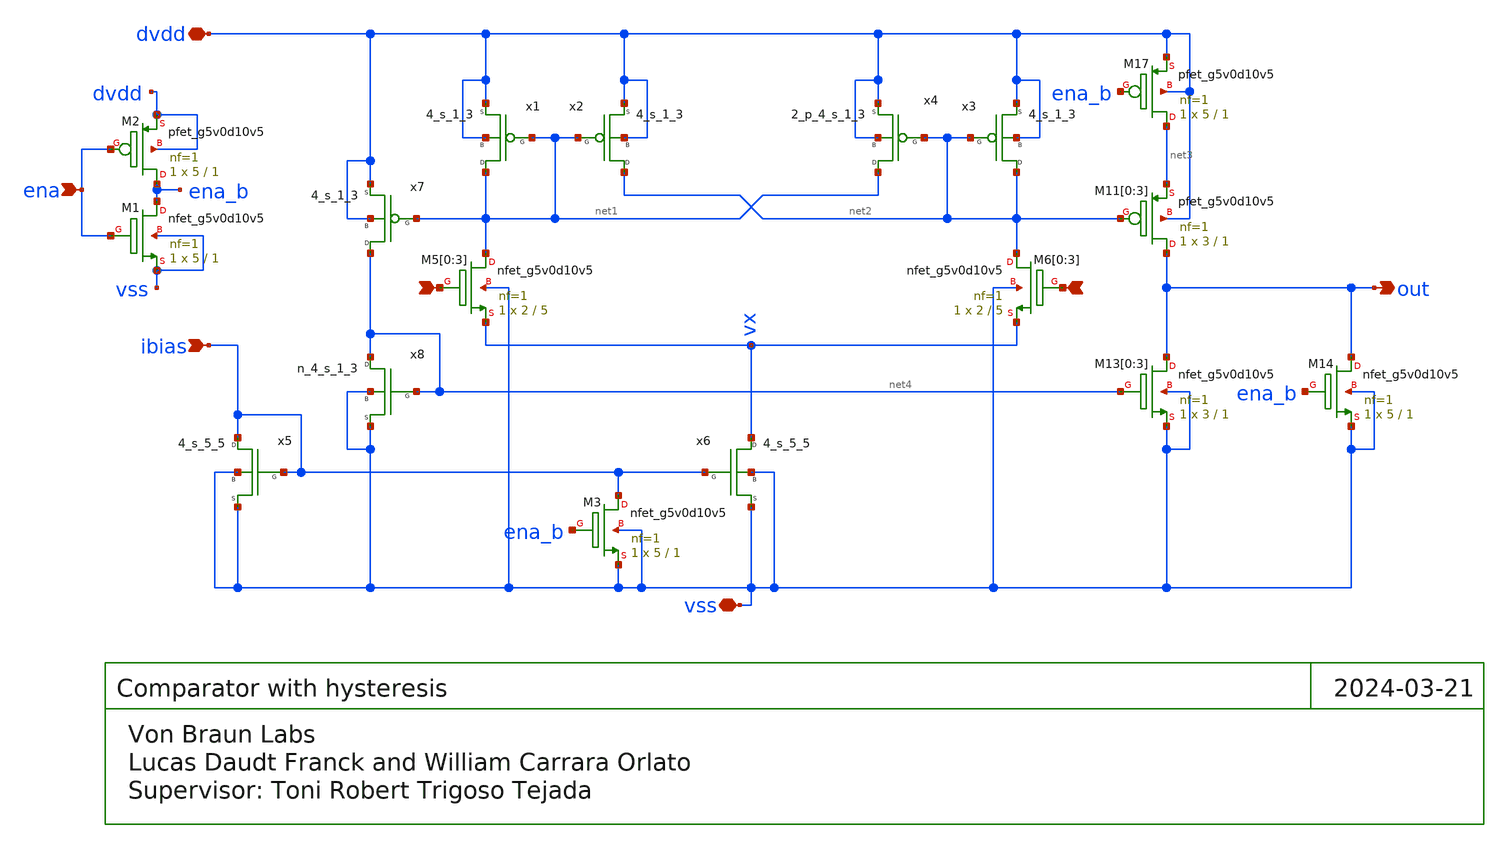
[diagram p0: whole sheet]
** sch_path: xschem/comp_hyst.sch
**.subckt comp_hyst dvdd - + out ibias ena vss
*.iopin dvdd
*.ipin -
*.ipin +
*.opin out
*.ipin ibias
*.ipin ena
*.iopin vss
XM17 net3 ena_b dvdd dvdd sky130_fd_pr__pfet_g5v0d10v5 L=1 W=5 nf=1 ad='int((nf+1)/2) * W/nf * 0.29'
+ as='int((nf+2)/2) * W/nf * 0.29' pd='2*int((nf+1)/2) * (W/nf + 0.29)' ps='2*int((nf+2)/2) * (W/nf + 0.29)'
+ nrd='0.29 / W' nrs='0.29 / W' sa=0 sb=0 sd=0 mult=1 m=1
XM11[0] out net2 net3 dvdd sky130_fd_pr__pfet_g5v0d10v5 L=1 W=3 nf=1 ad='int((nf+1)/2) * W/nf * 0.29'
+ as='int((nf+2)/2) * W/nf * 0.29' pd='2*int((nf+1)/2) * (W/nf + 0.29)' ps='2*int((nf+2)/2) * (W/nf + 0.29)'
+ nrd='0.29 / W' nrs='0.29 / W' sa=0 sb=0 sd=0 mult=1 m=1
XM11[1] out net2 net3 dvdd sky130_fd_pr__pfet_g5v0d10v5 L=1 W=3 nf=1 ad='int((nf+1)/2) * W/nf * 0.29'
+ as='int((nf+2)/2) * W/nf * 0.29' pd='2*int((nf+1)/2) * (W/nf + 0.29)' ps='2*int((nf+2)/2) * (W/nf + 0.29)'
+ nrd='0.29 / W' nrs='0.29 / W' sa=0 sb=0 sd=0 mult=1 m=1
XM11[2] out net2 net3 dvdd sky130_fd_pr__pfet_g5v0d10v5 L=1 W=3 nf=1 ad='int((nf+1)/2) * W/nf * 0.29'
+ as='int((nf+2)/2) * W/nf * 0.29' pd='2*int((nf+1)/2) * (W/nf + 0.29)' ps='2*int((nf+2)/2) * (W/nf + 0.29)'
+ nrd='0.29 / W' nrs='0.29 / W' sa=0 sb=0 sd=0 mult=1 m=1
XM11[3] out net2 net3 dvdd sky130_fd_pr__pfet_g5v0d10v5 L=1 W=3 nf=1 ad='int((nf+1)/2) * W/nf * 0.29'
+ as='int((nf+2)/2) * W/nf * 0.29' pd='2*int((nf+1)/2) * (W/nf + 0.29)' ps='2*int((nf+2)/2) * (W/nf + 0.29)'
+ nrd='0.29 / W' nrs='0.29 / W' sa=0 sb=0 sd=0 mult=1 m=1
XM13[0] out net4 vss vss sky130_fd_pr__nfet_g5v0d10v5 L=1 W=3 nf=1 ad='int((nf+1)/2) * W/nf * 0.29' as='int((nf+2)/2) * W/nf * 0.29'
+ pd='2*int((nf+1)/2) * (W/nf + 0.29)' ps='2*int((nf+2)/2) * (W/nf + 0.29)' nrd='0.29 / W' nrs='0.29 / W'
+ sa=0 sb=0 sd=0 mult=1 m=1
XM13[1] out net4 vss vss sky130_fd_pr__nfet_g5v0d10v5 L=1 W=3 nf=1 ad='int((nf+1)/2) * W/nf * 0.29' as='int((nf+2)/2) * W/nf * 0.29'
+ pd='2*int((nf+1)/2) * (W/nf + 0.29)' ps='2*int((nf+2)/2) * (W/nf + 0.29)' nrd='0.29 / W' nrs='0.29 / W'
+ sa=0 sb=0 sd=0 mult=1 m=1
XM13[2] out net4 vss vss sky130_fd_pr__nfet_g5v0d10v5 L=1 W=3 nf=1 ad='int((nf+1)/2) * W/nf * 0.29' as='int((nf+2)/2) * W/nf * 0.29'
+ pd='2*int((nf+1)/2) * (W/nf + 0.29)' ps='2*int((nf+2)/2) * (W/nf + 0.29)' nrd='0.29 / W' nrs='0.29 / W'
+ sa=0 sb=0 sd=0 mult=1 m=1
XM13[3] out net4 vss vss sky130_fd_pr__nfet_g5v0d10v5 L=1 W=3 nf=1 ad='int((nf+1)/2) * W/nf * 0.29' as='int((nf+2)/2) * W/nf * 0.29'
+ pd='2*int((nf+1)/2) * (W/nf + 0.29)' ps='2*int((nf+2)/2) * (W/nf + 0.29)' nrd='0.29 / W' nrs='0.29 / W'
+ sa=0 sb=0 sd=0 mult=1 m=1
XM14 out ena_b vss vss sky130_fd_pr__nfet_g5v0d10v5 L=1 W=5 nf=1 ad='int((nf+1)/2) * W/nf * 0.29' as='int((nf+2)/2) * W/nf * 0.29'
+ pd='2*int((nf+1)/2) * (W/nf + 0.29)' ps='2*int((nf+2)/2) * (W/nf + 0.29)' nrd='0.29 / W' nrs='0.29 / W'
+ sa=0 sb=0 sd=0 mult=1 m=1
XM5[0] net1 - vx vss sky130_fd_pr__nfet_g5v0d10v5 L=5 W=2 nf=1 ad='int((nf+1)/2) * W/nf * 0.29' as='int((nf+2)/2) * W/nf * 0.29'
+ pd='2*int((nf+1)/2) * (W/nf + 0.29)' ps='2*int((nf+2)/2) * (W/nf + 0.29)' nrd='0.29 / W' nrs='0.29 / W'
+ sa=0 sb=0 sd=0 mult=1 m=1
XM5[1] net1 - vx vss sky130_fd_pr__nfet_g5v0d10v5 L=5 W=2 nf=1 ad='int((nf+1)/2) * W/nf * 0.29' as='int((nf+2)/2) * W/nf * 0.29'
+ pd='2*int((nf+1)/2) * (W/nf + 0.29)' ps='2*int((nf+2)/2) * (W/nf + 0.29)' nrd='0.29 / W' nrs='0.29 / W'
+ sa=0 sb=0 sd=0 mult=1 m=1
XM5[2] net1 - vx vss sky130_fd_pr__nfet_g5v0d10v5 L=5 W=2 nf=1 ad='int((nf+1)/2) * W/nf * 0.29' as='int((nf+2)/2) * W/nf * 0.29'
+ pd='2*int((nf+1)/2) * (W/nf + 0.29)' ps='2*int((nf+2)/2) * (W/nf + 0.29)' nrd='0.29 / W' nrs='0.29 / W'
+ sa=0 sb=0 sd=0 mult=1 m=1
XM5[3] net1 - vx vss sky130_fd_pr__nfet_g5v0d10v5 L=5 W=2 nf=1 ad='int((nf+1)/2) * W/nf * 0.29' as='int((nf+2)/2) * W/nf * 0.29'
+ pd='2*int((nf+1)/2) * (W/nf + 0.29)' ps='2*int((nf+2)/2) * (W/nf + 0.29)' nrd='0.29 / W' nrs='0.29 / W'
+ sa=0 sb=0 sd=0 mult=1 m=1
XM6[0] net2 + vx vss sky130_fd_pr__nfet_g5v0d10v5 L=5 W=2 nf=1 ad='int((nf+1)/2) * W/nf * 0.29' as='int((nf+2)/2) * W/nf * 0.29'
+ pd='2*int((nf+1)/2) * (W/nf + 0.29)' ps='2*int((nf+2)/2) * (W/nf + 0.29)' nrd='0.29 / W' nrs='0.29 / W'
+ sa=0 sb=0 sd=0 mult=1 m=1
XM6[1] net2 + vx vss sky130_fd_pr__nfet_g5v0d10v5 L=5 W=2 nf=1 ad='int((nf+1)/2) * W/nf * 0.29' as='int((nf+2)/2) * W/nf * 0.29'
+ pd='2*int((nf+1)/2) * (W/nf + 0.29)' ps='2*int((nf+2)/2) * (W/nf + 0.29)' nrd='0.29 / W' nrs='0.29 / W'
+ sa=0 sb=0 sd=0 mult=1 m=1
XM6[2] net2 + vx vss sky130_fd_pr__nfet_g5v0d10v5 L=5 W=2 nf=1 ad='int((nf+1)/2) * W/nf * 0.29' as='int((nf+2)/2) * W/nf * 0.29'
+ pd='2*int((nf+1)/2) * (W/nf + 0.29)' ps='2*int((nf+2)/2) * (W/nf + 0.29)' nrd='0.29 / W' nrs='0.29 / W'
+ sa=0 sb=0 sd=0 mult=1 m=1
XM6[3] net2 + vx vss sky130_fd_pr__nfet_g5v0d10v5 L=5 W=2 nf=1 ad='int((nf+1)/2) * W/nf * 0.29' as='int((nf+2)/2) * W/nf * 0.29'
+ pd='2*int((nf+1)/2) * (W/nf + 0.29)' ps='2*int((nf+2)/2) * (W/nf + 0.29)' nrd='0.29 / W' nrs='0.29 / W'
+ sa=0 sb=0 sd=0 mult=1 m=1
x4 net1 dvdd net2 dvdd 2_p_4_s_1_3
x5 ibias vss ibias vss 4_s_5_5
x6 vx vss ibias vss 4_s_5_5
x1 net1 dvdd net1 dvdd 4_s_1_3
x2 net2 dvdd net1 dvdd 4_s_1_3
x3 net2 dvdd net2 dvdd 4_s_1_3
x7 net4 dvdd net1 dvdd 4_s_1_3
x8 net4 vss net4 vss n_4_s_1_3
XM3 ibias ena_b vss vss sky130_fd_pr__nfet_g5v0d10v5 L=1 W=5 nf=1 ad='int((nf+1)/2) * W/nf * 0.29' as='int((nf+2)/2) * W/nf * 0.29'
+ pd='2*int((nf+1)/2) * (W/nf + 0.29)' ps='2*int((nf+2)/2) * (W/nf + 0.29)' nrd='0.29 / W' nrs='0.29 / W'
+ sa=0 sb=0 sd=0 mult=1 m=1
XM1 ena_b ena vss vss sky130_fd_pr__nfet_g5v0d10v5 L=1 W=5 nf=1 ad='int((nf+1)/2) * W/nf * 0.29' as='int((nf+2)/2) * W/nf * 0.29'
+ pd='2*int((nf+1)/2) * (W/nf + 0.29)' ps='2*int((nf+2)/2) * (W/nf + 0.29)' nrd='0.29 / W' nrs='0.29 / W'
+ sa=0 sb=0 sd=0 mult=1 m=1
XM2 ena_b ena dvdd dvdd sky130_fd_pr__pfet_g5v0d10v5 L=1 W=5 nf=1 ad='int((nf+1)/2) * W/nf * 0.29' as='int((nf+2)/2) * W/nf * 0.29'
+ pd='2*int((nf+1)/2) * (W/nf + 0.29)' ps='2*int((nf+2)/2) * (W/nf + 0.29)' nrd='0.29 / W' nrs='0.29 / W'
+ sa=0 sb=0 sd=0 mult=1 m=1
**.ends

* expanding   symbol:  2_p_4_s_1_3.sym # of pins=4
** sym_path: xschem/2_p_4_s_1_3.sym
** sch_path: xschem/2_p_4_s_1_3.sch
.subckt 2_p_4_s_1_3 D B G S
*.iopin D
*.iopin B
*.iopin G
*.iopin S
XM1 net1 G net2 B sky130_fd_pr__pfet_g5v0d10v5 L=3 W=1 nf=1 ad='int((nf+1)/2) * W/nf * 0.29' as='int((nf+2)/2) * W/nf * 0.29'
+ pd='2*int((nf+1)/2) * (W/nf + 0.29)' ps='2*int((nf+2)/2) * (W/nf + 0.29)' nrd='0.29 / W' nrs='0.29 / W'
+ sa=0 sb=0 sd=0 mult=2 m=2
XM2 net3 G S B sky130_fd_pr__pfet_g5v0d10v5 L=3 W=1 nf=1 ad='int((nf+1)/2) * W/nf * 0.29' as='int((nf+2)/2) * W/nf * 0.29'
+ pd='2*int((nf+1)/2) * (W/nf + 0.29)' ps='2*int((nf+2)/2) * (W/nf + 0.29)' nrd='0.29 / W' nrs='0.29 / W'
+ sa=0 sb=0 sd=0 mult=2 m=2
XM3 D G net1 B sky130_fd_pr__pfet_g5v0d10v5 L=3 W=1 nf=1 ad='int((nf+1)/2) * W/nf * 0.29' as='int((nf+2)/2) * W/nf * 0.29'
+ pd='2*int((nf+1)/2) * (W/nf + 0.29)' ps='2*int((nf+2)/2) * (W/nf + 0.29)' nrd='0.29 / W' nrs='0.29 / W'
+ sa=0 sb=0 sd=0 mult=2 m=2
XM4 net2 G net3 B sky130_fd_pr__pfet_g5v0d10v5 L=3 W=1 nf=1 ad='int((nf+1)/2) * W/nf * 0.29' as='int((nf+2)/2) * W/nf * 0.29'
+ pd='2*int((nf+1)/2) * (W/nf + 0.29)' ps='2*int((nf+2)/2) * (W/nf + 0.29)' nrd='0.29 / W' nrs='0.29 / W'
+ sa=0 sb=0 sd=0 mult=2 m=2
.ends


* expanding   symbol:  4_s_5_5.sym # of pins=4
** sym_path: xschem/4_s_5_5.sym
** sch_path: xschem/4_s_5_5.sch
.subckt 4_s_5_5 D B G S
*.iopin S
*.iopin D
*.iopin B
*.iopin G
XM1 D G net1 B sky130_fd_pr__nfet_g5v0d10v5 L=5 W=5 nf=1 ad='int((nf+1)/2) * W/nf * 0.29' as='int((nf+2)/2) * W/nf * 0.29'
+ pd='2*int((nf+1)/2) * (W/nf + 0.29)' ps='2*int((nf+2)/2) * (W/nf + 0.29)' nrd='0.29 / W' nrs='0.29 / W'
+ sa=0 sb=0 sd=0 mult=1 m=1
XM2 net1 G net2 B sky130_fd_pr__nfet_g5v0d10v5 L=5 W=5 nf=1 ad='int((nf+1)/2) * W/nf * 0.29' as='int((nf+2)/2) * W/nf * 0.29'
+ pd='2*int((nf+1)/2) * (W/nf + 0.29)' ps='2*int((nf+2)/2) * (W/nf + 0.29)' nrd='0.29 / W' nrs='0.29 / W'
+ sa=0 sb=0 sd=0 mult=1 m=1
XM3 net2 G net3 B sky130_fd_pr__nfet_g5v0d10v5 L=5 W=5 nf=1 ad='int((nf+1)/2) * W/nf * 0.29' as='int((nf+2)/2) * W/nf * 0.29'
+ pd='2*int((nf+1)/2) * (W/nf + 0.29)' ps='2*int((nf+2)/2) * (W/nf + 0.29)' nrd='0.29 / W' nrs='0.29 / W'
+ sa=0 sb=0 sd=0 mult=1 m=1
XM4 net3 G S B sky130_fd_pr__nfet_g5v0d10v5 L=5 W=5 nf=1 ad='int((nf+1)/2) * W/nf * 0.29' as='int((nf+2)/2) * W/nf * 0.29'
+ pd='2*int((nf+1)/2) * (W/nf + 0.29)' ps='2*int((nf+2)/2) * (W/nf + 0.29)' nrd='0.29 / W' nrs='0.29 / W'
+ sa=0 sb=0 sd=0 mult=1 m=1
.ends


* expanding   symbol:  4_s_1_3.sym # of pins=4
** sym_path: xschem/4_s_1_3.sym
** sch_path: xschem/4_s_1_3.sch
.subckt 4_s_1_3 D B G S
*.iopin S
*.iopin D
*.iopin B
*.iopin G
XM1 net1 G net2 B sky130_fd_pr__pfet_g5v0d10v5 L=3 W=1 nf=1 ad='int((nf+1)/2) * W/nf * 0.29' as='int((nf+2)/2) * W/nf * 0.29'
+ pd='2*int((nf+1)/2) * (W/nf + 0.29)' ps='2*int((nf+2)/2) * (W/nf + 0.29)' nrd='0.29 / W' nrs='0.29 / W'
+ sa=0 sb=0 sd=0 mult=1 m=1
XM2 net3 G S B sky130_fd_pr__pfet_g5v0d10v5 L=3 W=1 nf=1 ad='int((nf+1)/2) * W/nf * 0.29' as='int((nf+2)/2) * W/nf * 0.29'
+ pd='2*int((nf+1)/2) * (W/nf + 0.29)' ps='2*int((nf+2)/2) * (W/nf + 0.29)' nrd='0.29 / W' nrs='0.29 / W'
+ sa=0 sb=0 sd=0 mult=1 m=1
XM3 D G net1 B sky130_fd_pr__pfet_g5v0d10v5 L=3 W=1 nf=1 ad='int((nf+1)/2) * W/nf * 0.29' as='int((nf+2)/2) * W/nf * 0.29'
+ pd='2*int((nf+1)/2) * (W/nf + 0.29)' ps='2*int((nf+2)/2) * (W/nf + 0.29)' nrd='0.29 / W' nrs='0.29 / W'
+ sa=0 sb=0 sd=0 mult=1 m=1
XM4 net2 G net3 B sky130_fd_pr__pfet_g5v0d10v5 L=3 W=1 nf=1 ad='int((nf+1)/2) * W/nf * 0.29' as='int((nf+2)/2) * W/nf * 0.29'
+ pd='2*int((nf+1)/2) * (W/nf + 0.29)' ps='2*int((nf+2)/2) * (W/nf + 0.29)' nrd='0.29 / W' nrs='0.29 / W'
+ sa=0 sb=0 sd=0 mult=1 m=1
.ends


* expanding   symbol:  n_4_s_1_3.sym # of pins=4
** sym_path: xschem/n_4_s_1_3.sym
** sch_path: xschem/n_4_s_1_3.sch
.subckt n_4_s_1_3 D B G S
*.iopin S
*.iopin D
*.iopin B
*.iopin G
XM1 net2 G net1 B sky130_fd_pr__nfet_g5v0d10v5 L=3 W=1 nf=1 ad='int((nf+1)/2) * W/nf * 0.29' as='int((nf+2)/2) * W/nf * 0.29'
+ pd='2*int((nf+1)/2) * (W/nf + 0.29)' ps='2*int((nf+2)/2) * (W/nf + 0.29)' nrd='0.29 / W' nrs='0.29 / W'
+ sa=0 sb=0 sd=0 mult=1 m=1
XM2 S G net3 B sky130_fd_pr__nfet_g5v0d10v5 L=3 W=1 nf=1 ad='int((nf+1)/2) * W/nf * 0.29' as='int((nf+2)/2) * W/nf * 0.29'
+ pd='2*int((nf+1)/2) * (W/nf + 0.29)' ps='2*int((nf+2)/2) * (W/nf + 0.29)' nrd='0.29 / W' nrs='0.29 / W'
+ sa=0 sb=0 sd=0 mult=1 m=1
XM3 net1 G D B sky130_fd_pr__nfet_g5v0d10v5 L=3 W=1 nf=1 ad='int((nf+1)/2) * W/nf * 0.29' as='int((nf+2)/2) * W/nf * 0.29'
+ pd='2*int((nf+1)/2) * (W/nf + 0.29)' ps='2*int((nf+2)/2) * (W/nf + 0.29)' nrd='0.29 / W' nrs='0.29 / W'
+ sa=0 sb=0 sd=0 mult=1 m=1
XM4 net3 G net2 B sky130_fd_pr__nfet_g5v0d10v5 L=3 W=1 nf=1 ad='int((nf+1)/2) * W/nf * 0.29' as='int((nf+2)/2) * W/nf * 0.29'
+ pd='2*int((nf+1)/2) * (W/nf + 0.29)' ps='2*int((nf+2)/2) * (W/nf + 0.29)' nrd='0.29 / W' nrs='0.29 / W'
+ sa=0 sb=0 sd=0 mult=1 m=1
.ends

.end
